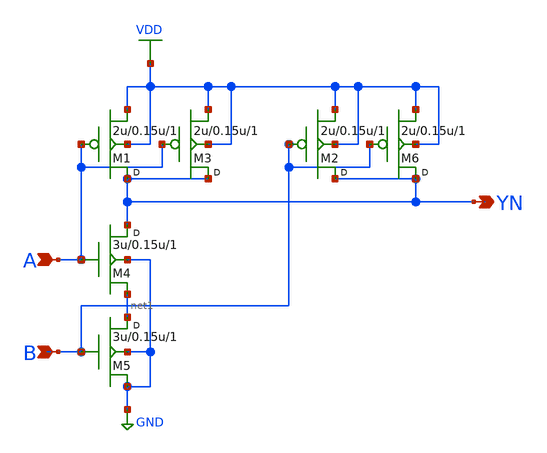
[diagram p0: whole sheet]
** sch_path: lib/xschem/schematics/NAND2X2.sch
**.subckt NAND2X2 A B YN
*.ipin A
*.ipin B
*.opin YN
M1 YN A VDD VDD pmos w=2u l=0.15u m=1
M2 YN B VDD VDD pmos w=2u l=0.15u m=1
M4 YN A net1 GND nmos w=3u l=0.15u m=1
M5 net1 B GND GND nmos w=3u l=0.15u m=1
M3 YN A VDD VDD pmos w=2u l=0.15u m=1
M6 YN B VDD VDD pmos w=2u l=0.15u m=1
**.ends
.GLOBAL GND
.GLOBAL VDD
.end
